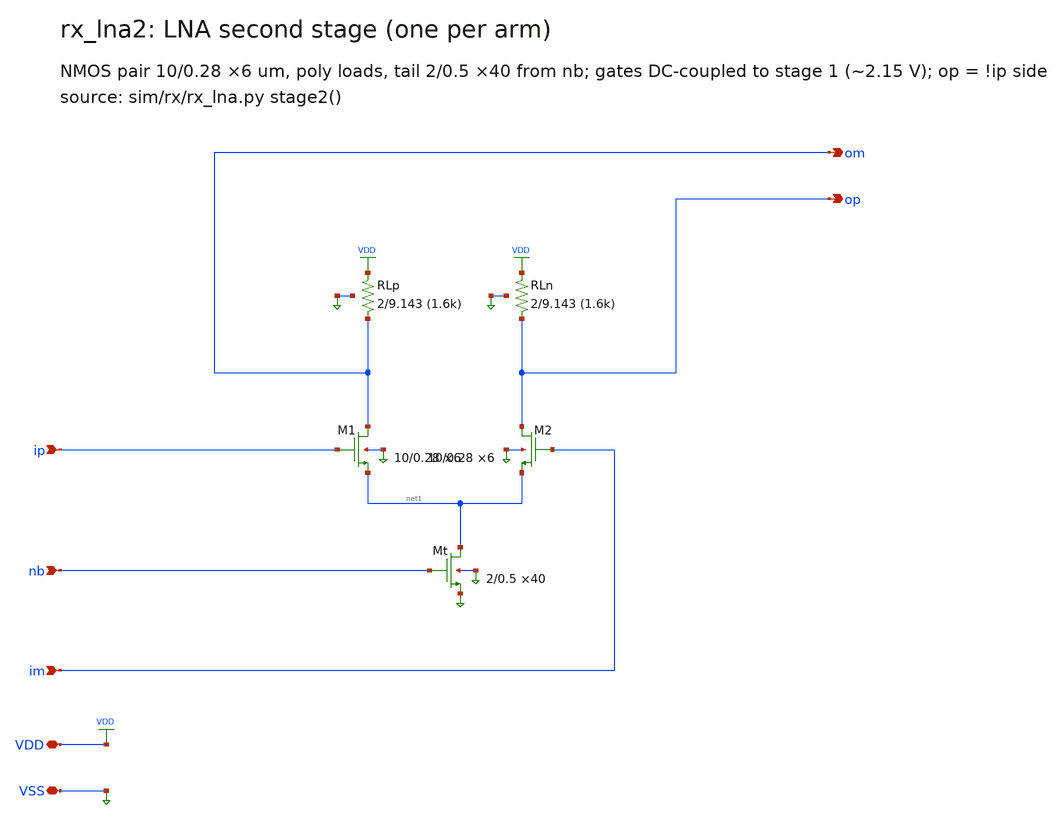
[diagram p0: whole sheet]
** sch_path: xschem/rx_lna2.sch
**.subckt rx_lna2 VDD VSS ip im op om nb
*.iopin VDD
*.iopin VSS
*.ipin ip
*.ipin im
*.opin op
*.opin om
*.ipin nb
XM1 om ip net1 VSS nfet_03v3 L=0.28u W=10.0u nf=1 ad=5.0p as=5.0p pd=21.0u ps=21.0u nrd=0 nrs=0 sa=0
+ sb=0 sd=0 m=6
XM2 op im net1 VSS nfet_03v3 L=0.28u W=10.0u nf=1 ad=5.0p as=5.0p pd=21.0u ps=21.0u nrd=0 nrs=0 sa=0
+ sb=0 sd=0 m=6
XMt net1 nb VSS VSS nfet_03v3 L=0.5u W=2.0u nf=1 ad=1.0p as=1.0p pd=5.0u ps=5.0u nrd=0 nrs=0 sa=0
+ sb=0 sd=0 m=40
XRLp om VDD VSS ppolyf_u r_width=2.0e-6 r_length=9.143e-6 m=1
XRLn op VDD VSS ppolyf_u r_width=2.0e-6 r_length=9.143e-6 m=1
**.ends
.end
